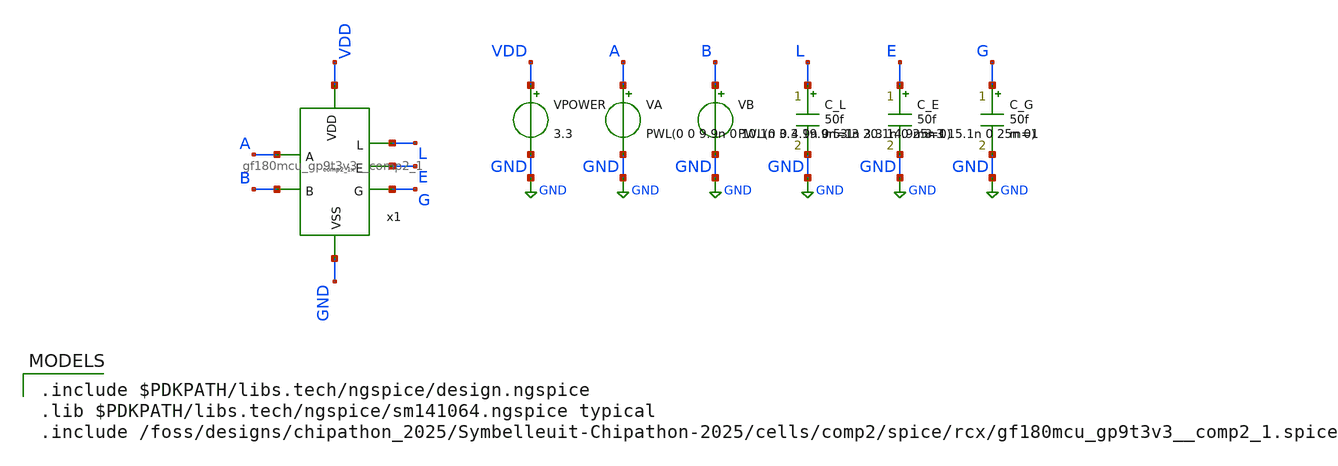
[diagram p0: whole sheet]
** sch_path: cells/comp2/cace/templates/comp2_tb_dynamic_power.sch
**.subckt comp2_tb_dynamic_power
x1 VDD L A E G B GND gf180mcu_gp9t3v3__comp2_1
VPOWER VDD GND 3.3
.save i(vpower)
VA A GND PWL(0 0 9.9n 0 10.1n 3.3 19.9n 3.3 20.1n 0 25n 0)
VB B GND PWL(0 0 4.9n 0 5.1n 3.3 14.9n 3.3 15.1n 0 25n 0)
C_L L GND 50f m=1
C_E E GND 50f m=1
C_G G GND 50f m=1
**** begin user architecture code

.include $PDKPATH/libs.tech/ngspice/design.ngspice
.lib $PDKPATH/libs.tech/ngspice/sm141064.ngspice typical
.include /foss/designs/chipathon_2025/Symbelleuit-Chipathon-2025/cells/comp2/spice/rcx/gf180mcu_gp9t3v3__comp2_1.spice


* CACE Dynamic Average Power Simulation
.tran 100p 25n
.control
  run
  let idd = -i(VPOWER)
  meas tran i_avg AVG idd from=1n to=25n
  let p_dynamic = i_avg * 3.3
  print p_dynamic
  echo $&p_dynamic > comp2_tb_dynamic_power_0.data
.endc
.GLOBAL GND


**** end user architecture code
**.ends
.GLOBAL GND
.end
